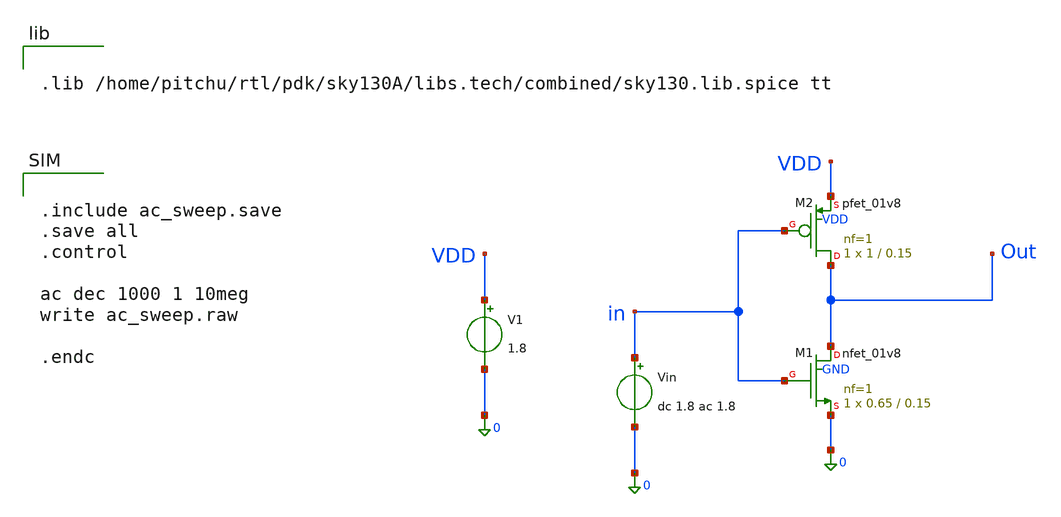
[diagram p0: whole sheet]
** sch_path: experiments/ac_sweep.sch
**.subckt ac_sweep
XM1 Out in 0 GND sky130_fd_pr__nfet_01v8 L=0.15 W=0.65 nf=1 ad='int((1 + 1)/2) * 0.65 / 1 * 0.29' as='int((1 + 2)/2) * 0.65 / 1 * 0.29'
+ pd='2*int((1 + 1)/2) * (0.65 / 1 + 0.29)' ps='2*int((1 + 2)/2) * (0.65 / 1 + 0.29)' nrd='0.29 / 0.65 '
+ nrs='0.29 / 0.65 ' sa=0 sb=0 sd=0 mult=1 m=1
XM2 Out in VDD VDD sky130_fd_pr__pfet_01v8 L=0.15 W=1 nf=1 ad='int((1 + 1)/2) * 1 / 1 * 0.29' as='int((1 + 2)/2) * 1 / 1 * 0.29'
+ pd='2*int((1 + 1)/2) * (1 / 1 + 0.29)' ps='2*int((1 + 2)/2) * (1 / 1 + 0.29)' nrd='0.29 / 1 ' nrs='0.29 / 1 '
+ sa=0 sb=0 sd=0 mult=1 m=1
Vin in 0 dc 1.8 ac 1.8
.save i(vin)
V1 VDD 0 1.8
**** begin user architecture code


.include ac_sweep.save
.save all
.control

ac dec 1000 1 10meg
write ac_sweep.raw

.endc




.lib /home/pitchu/rtl/pdk/sky130A/libs.tech/combined/sky130.lib.spice tt


**** end user architecture code
**.ends
.end
